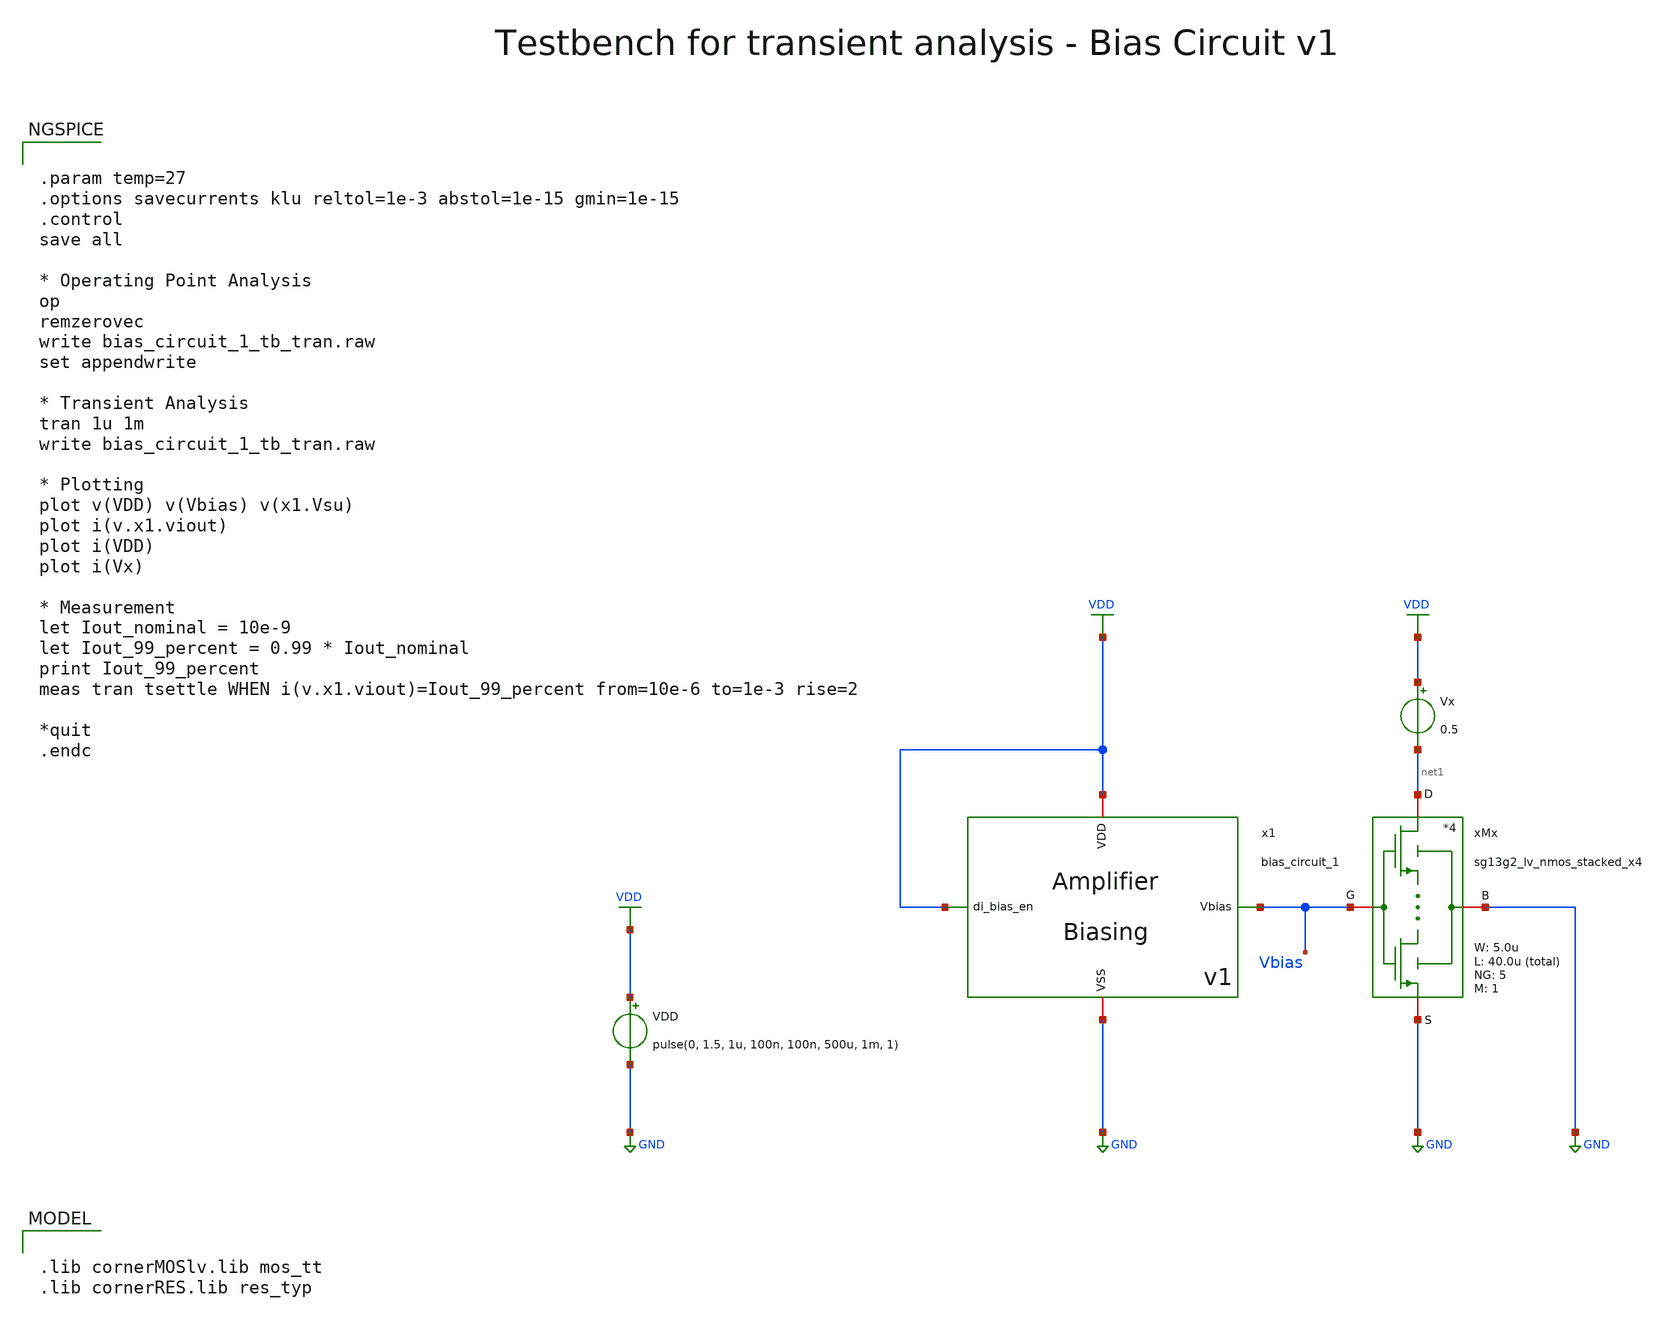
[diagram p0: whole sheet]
** sch_path: SG13G2_ATBS-ADC-main/xschem/bio_amplifier/amplifier_core/bias_circuit/bias_circuit_1/testbenches/bias_circuit_1_tb_tran.sch
**.subckt bias_circuit_1_tb_tran
VDD VDD GND pulse(0, 1.5, 1u, 100n, 100n, 500u, 1m, 1)
xMx net1 Vbias GND GND sg13g2_lv_nmos_stacked_x4 W_N=5.0u L_N=40.0u NG_N=5 M_N=1
Vx VDD net1 0.5
x1 VDD Vbias VDD GND bias_circuit_1
**** begin user architecture code

.lib cornerMOSlv.lib mos_tt
.lib cornerRES.lib res_typ



.param temp=27
.options savecurrents klu reltol=1e-3 abstol=1e-15 gmin=1e-15
.control
save all

* Operating Point Analysis
op
remzerovec
write bias_circuit_1_tb_tran.raw
set appendwrite

* Transient Analysis
tran 1u 1m
write bias_circuit_1_tb_tran.raw

* Plotting
plot v(VDD) v(Vbias) v(x1.Vsu)
plot i(v.x1.viout)
plot i(VDD)
plot i(Vx)

* Measurement
let Iout_nominal = 10e-9
let Iout_99_percent = 0.99 * Iout_nominal
print Iout_99_percent
meas tran tsettle WHEN i(v.x1.viout)=Iout_99_percent from=10e-6 to=1e-3 rise=2

*quit
.endc

**** end user architecture code
**.ends
.GLOBAL GND
.GLOBAL VDD
.end
